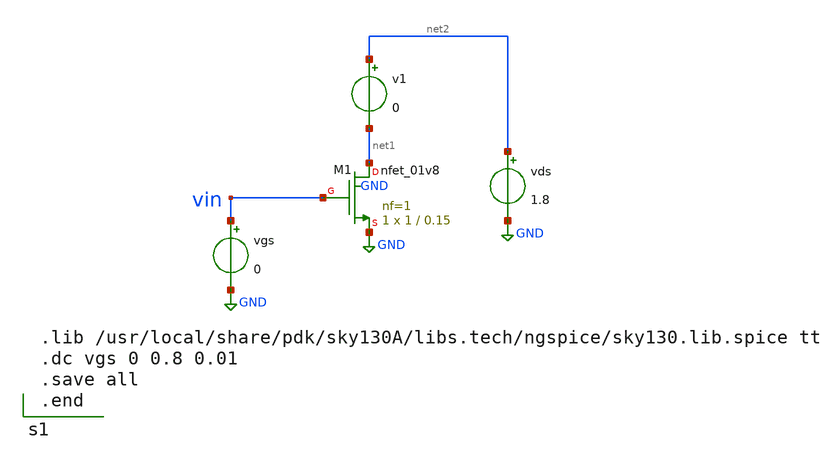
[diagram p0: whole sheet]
** sch_path: XSCHEM/nmos_id_vgs/nmos_id_vgs.sch
* Copyright 2021 Stefan Frederik Schippers
* Licensed under the Apache License, Version 2.0 (the "License");
* you may not use this file except in compliance with the License.
* You may obtain a copy of the License at
* https://www.apache.org/licenses/LICENSE-2.0
* Unless required by applicable law or agreed to in writing, software
* distributed under the License is distributed on an "AS IS" BASIS,
* WITHOUT WARRANTIES OR CONDITIONS OF ANY KIND, either express or implied.
* See the License for the specific language governing permissions and
* limitations under the License.
**.subckt nmos_id_vgs
XM1 net1 vin GND GND sky130_fd_pr__nfet_01v8 L=0.15 W=1 nf=1 ad='int((nf+1)/2) * W/nf * 0.29' as='int((nf+2)/2) * W/nf * 0.29'
+ pd='2*int((nf+1)/2) * (W/nf + 0.29)' ps='2*int((nf+2)/2) * (W/nf + 0.29)' nrd='0.29 / W' nrs='0.29 / W'
+ sa=0 sb=0 sd=0 mult=1 m=1
vgs vin GND 0
vds net2 GND 1.8
v1 net2 net1 0
**** begin user architecture code

.lib /usr/local/share/pdk/sky130A/libs.tech/ngspice/sky130.lib.spice tt
.dc vgs 0 0.8 0.01
.save all
.end

**** end user architecture code
**.ends
.GLOBAL GND
.end
